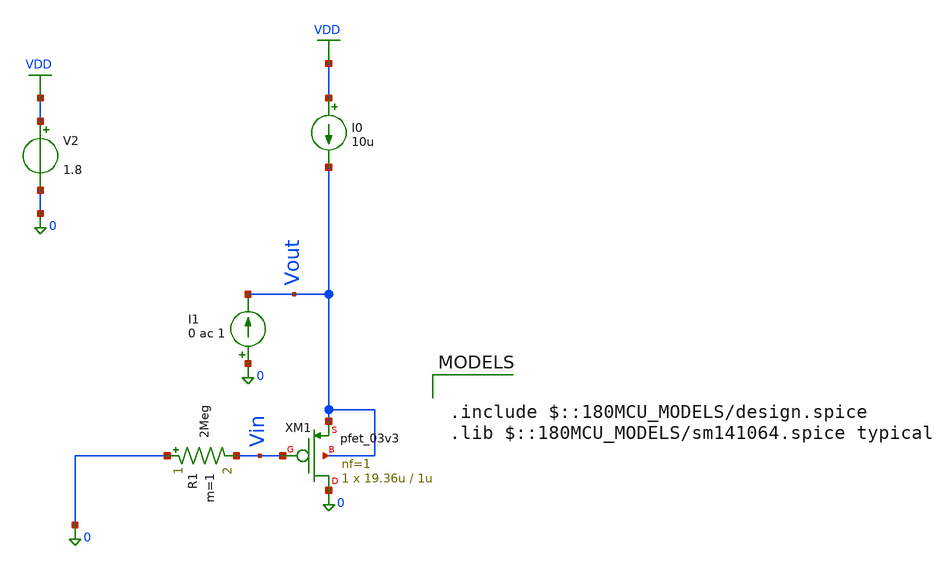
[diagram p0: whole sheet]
** sch_path: Lab_04/Zout_CD.sch
**.subckt Zout_CD
XM1 0 Vin Vout Vout pfet_03v3 L=1u W=19.36u nf=1 ad='int((nf+1)/2) * W/nf * 0.18u' as='int((nf+2)/2) * W/nf * 0.18u'
+ pd='2*int((nf+1)/2) * (W/nf + 0.18u)' ps='2*int((nf+2)/2) * (W/nf + 0.18u)' nrd='0.18u / W' nrs='0.18u / W'
+ sa=0 sb=0 sd=0 m=1
I0 VDD Vout 10u
R1 0 Vin 2Meg m=1
V2 VDD 0 1.8
I1 0 Vout 0 ac 1
**** begin user architecture code

.include $::180MCU_MODELS/design.spice
.lib $::180MCU_MODELS/sm141064.spice typical


.control
alterparam sw_stat_global = 0
alterparam sw_stat_mismatch = 0
reset
set outfile = zout_results.txt

* Increased to 100 points per decade for more accurate measurements
ac dec 100 1 10g
write cd_amp_zout.raw

echo "CD Amplifier Zout Sim Results" > $outfile

* --- 1. Your standard measurements ---
meas ac zout_low_freq FIND vmag(vout) AT=1k
meas ac zout_high_freq MAX vmag(vout)
echo "Zout @ 1kHz = $&zout_low_freq" >> $outfile
echo "Zout peak (max) = $&zout_high_freq" >> $outfile

* --- 2. Mathematical Calculation using OP values ---
let my_pi = 3.14159265359
let my_rsig = 2e6
let my_cgs = 49.57e-15
let my_gm = 100.8e-6

let fz_calc = 1 / (2 * my_pi * my_rsig * my_cgs)
let fp_calc = my_gm / (2 * my_pi * my_cgs)

echo "Calculated Math Zero (fz) = $&fz_calc Hz" >> $outfile
echo "Calculated Math Pole (fp) = $&fp_calc Hz" >> $outfile

* --- 3. Measure the Simulated Zero from the AC Curve ---
* The zero starts when the impedance magnitude increases by a factor of sqrt(2)
let zout_3db = zout_low_freq * 1.41421356
meas ac sim_zero WHEN vmag(vout)=zout_3db
echo "Simulated AC Curve Zero = $&sim_zero Hz" >> $outfile

.endc

**** end user architecture code
**.ends
.GLOBAL VDD
.end
